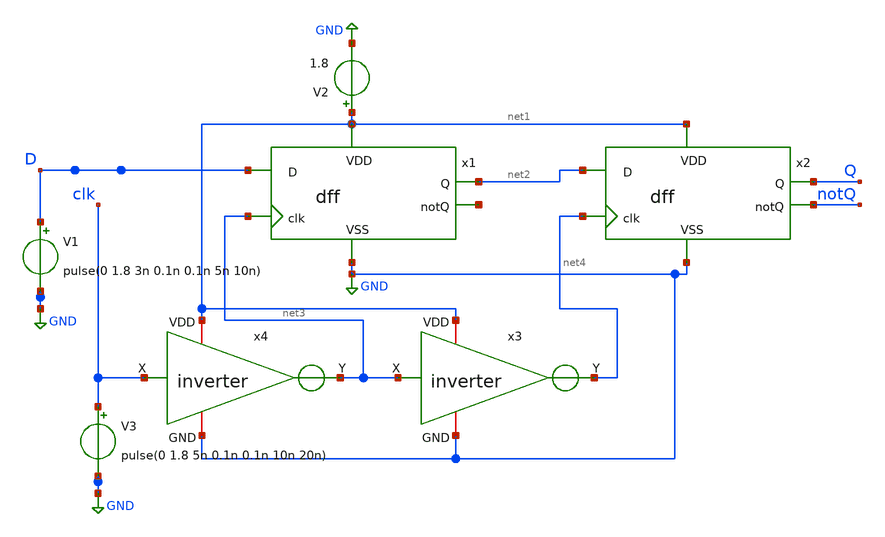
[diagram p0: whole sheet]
** sch_path: Layouts and Schematics/Spice Sim and Schem/dfftest.sch
**.subckt dfftest
V1 D GND pulse(0 1.8 3n 0.1n 0.1n 5n 10n)
V2 net1 GND 1.8
V3 clk GND pulse(0 1.8 5n 0.1n 0.1n 10n 20n)
x1 net1 net3 net2 D net5 GND dff
x2 net1 net4 Q net2 notQ GND dff
x3 net1 net3 net4 GND inv
x4 net1 clk net3 GND inv
**** begin user architecture code
 .lib $::SKYWATER_MODELS/sky130.lib.spice tt

.include /home/wyatt/EE431
.tran 1n 40n
.control
run
.endc

**** end user architecture code
**.ends
.GLOBAL GND
.end
